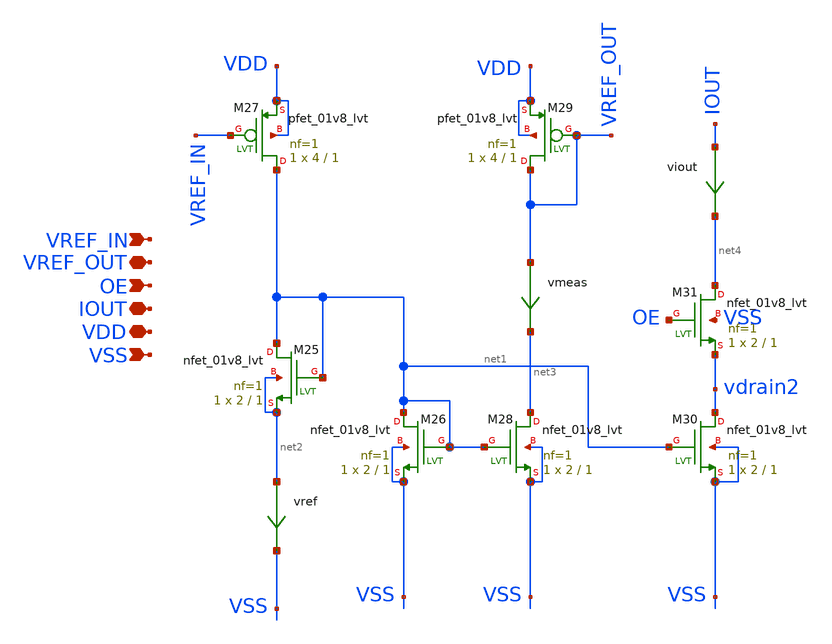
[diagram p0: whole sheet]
** sch_path: xschem/idac1cell.sch
**.subckt idac1cell VSS VREF_OUT VREF_IN VDD IOUT OE
*.ipin VSS
*.iopin VREF_OUT
*.ipin VREF_IN
*.iopin VDD
*.iopin IOUT
*.ipin OE
XM25 net1 net1 net2 net2 sky130_fd_pr__nfet_01v8_lvt L=1 W=2 nf=1 ad='int((nf+1)/2) * W/nf * 0.29' as='int((nf+2)/2) * W/nf * 0.29'
+ pd='2*int((nf+1)/2) * (W/nf + 0.29)' ps='2*int((nf+2)/2) * (W/nf + 0.29)' nrd='0.29 / W' nrs='0.29 / W'
+ sa=0 sb=0 sd=0 mult=1 m=1
XM26 net1 net1 VSS VSS sky130_fd_pr__nfet_01v8_lvt L=1 W=2 nf=1 ad='int((nf+1)/2) * W/nf * 0.29' as='int((nf+2)/2) * W/nf * 0.29'
+ pd='2*int((nf+1)/2) * (W/nf + 0.29)' ps='2*int((nf+2)/2) * (W/nf + 0.29)' nrd='0.29 / W' nrs='0.29 / W'
+ sa=0 sb=0 sd=0 mult=1 m=1
XM27 net1 VREF_IN VDD VDD sky130_fd_pr__pfet_01v8_lvt L=1 W=4 nf=1 ad='int((nf+1)/2) * W/nf * 0.29' as='int((nf+2)/2) * W/nf * 0.29'
+ pd='2*int((nf+1)/2) * (W/nf + 0.29)' ps='2*int((nf+2)/2) * (W/nf + 0.29)' nrd='0.29 / W' nrs='0.29 / W'
+ sa=0 sb=0 sd=0 mult=1 m=1
XM28 net3 net1 VSS VSS sky130_fd_pr__nfet_01v8_lvt L=1 W=2 nf=1 ad='int((nf+1)/2) * W/nf * 0.29' as='int((nf+2)/2) * W/nf * 0.29'
+ pd='2*int((nf+1)/2) * (W/nf + 0.29)' ps='2*int((nf+2)/2) * (W/nf + 0.29)' nrd='0.29 / W' nrs='0.29 / W'
+ sa=0 sb=0 sd=0 mult=1 m=1
XM29 VREF_OUT VREF_OUT VDD VDD sky130_fd_pr__pfet_01v8_lvt L=1 W=4 nf=1 ad='int((nf+1)/2) * W/nf * 0.29'
+ as='int((nf+2)/2) * W/nf * 0.29' pd='2*int((nf+1)/2) * (W/nf + 0.29)' ps='2*int((nf+2)/2) * (W/nf + 0.29)'
+ nrd='0.29 / W' nrs='0.29 / W' sa=0 sb=0 sd=0 mult=1 m=1
XM30 vdrain2 net1 VSS VSS sky130_fd_pr__nfet_01v8_lvt L=1 W=2 nf=1 ad='int((nf+1)/2) * W/nf * 0.29' as='int((nf+2)/2) * W/nf * 0.29'
+ pd='2*int((nf+1)/2) * (W/nf + 0.29)' ps='2*int((nf+2)/2) * (W/nf + 0.29)' nrd='0.29 / W' nrs='0.29 / W'
+ sa=0 sb=0 sd=0 mult=1 m=1
XM31 net4 OE vdrain2 VSS sky130_fd_pr__nfet_01v8_lvt L=1 W=2 nf=1 ad='int((nf+1)/2) * W/nf * 0.29' as='int((nf+2)/2) * W/nf * 0.29'
+ pd='2*int((nf+1)/2) * (W/nf + 0.29)' ps='2*int((nf+2)/2) * (W/nf + 0.29)' nrd='0.29 / W' nrs='0.29 / W'
+ sa=0 sb=0 sd=0 mult=1 m=1
vref net2 VSS 0
.save i(vref)
vmeas VREF_OUT net3 0
.save i(vmeas)
viout IOUT net4 0
.save i(viout)
**.ends
.end
